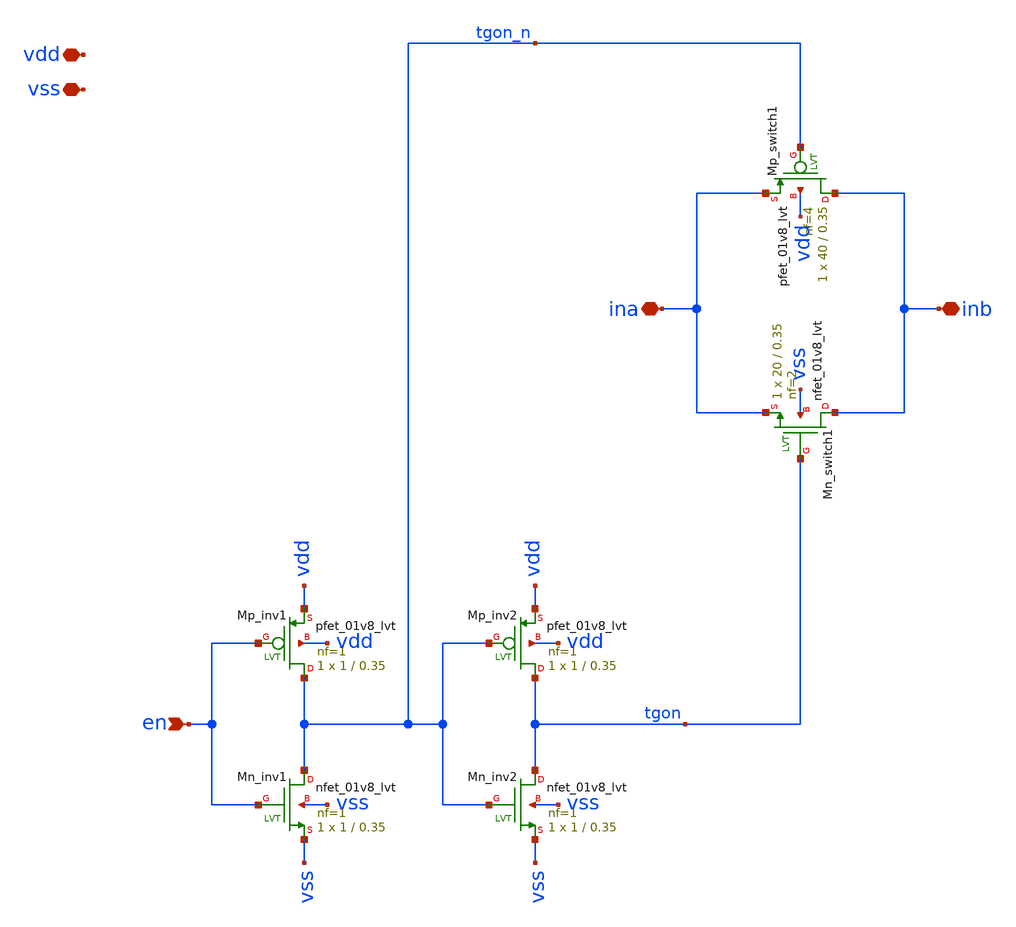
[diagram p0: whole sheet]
** sch_path: xsch/ip/tgates/tgate_1/tgate_1.sch
**.subckt tgate_1 vdd vss en inb ina
*.iopin vdd
*.iopin vss
*.ipin en
*.iopin inb
*.iopin ina
XMp_inv1 tgon_n en vdd vdd sky130_fd_pr__pfet_01v8_lvt L=0.35 W=1 nf=1 ad='int((nf+1)/2) * W/nf * 0.29'
+ as='int((nf+2)/2) * W/nf * 0.29' pd='2*int((nf+1)/2) * (W/nf + 0.29)' ps='2*int((nf+2)/2) * (W/nf + 0.29)'
+ nrd='0.29 / W' nrs='0.29 / W' sa=0 sb=0 sd=0 mult=1 m=1
XMn_inv1 tgon_n en vss vss sky130_fd_pr__nfet_01v8_lvt L=0.35 W=1 nf=1 ad='int((nf+1)/2) * W/nf * 0.29'
+ as='int((nf+2)/2) * W/nf * 0.29' pd='2*int((nf+1)/2) * (W/nf + 0.29)' ps='2*int((nf+2)/2) * (W/nf + 0.29)'
+ nrd='0.29 / W' nrs='0.29 / W' sa=0 sb=0 sd=0 mult=1 m=1
XMp_inv2 tgon tgon_n vdd vdd sky130_fd_pr__pfet_01v8_lvt L=0.35 W=1 nf=1 ad='int((nf+1)/2) * W/nf * 0.29'
+ as='int((nf+2)/2) * W/nf * 0.29' pd='2*int((nf+1)/2) * (W/nf + 0.29)' ps='2*int((nf+2)/2) * (W/nf + 0.29)'
+ nrd='0.29 / W' nrs='0.29 / W' sa=0 sb=0 sd=0 mult=1 m=1
XMn_inv2 tgon tgon_n vss vss sky130_fd_pr__nfet_01v8_lvt L=0.35 W=1 nf=1 ad='int((nf+1)/2) * W/nf * 0.29'
+ as='int((nf+2)/2) * W/nf * 0.29' pd='2*int((nf+1)/2) * (W/nf + 0.29)' ps='2*int((nf+2)/2) * (W/nf + 0.29)'
+ nrd='0.29 / W' nrs='0.29 / W' sa=0 sb=0 sd=0 mult=1 m=1
XMn_switch1 inb tgon ina vss sky130_fd_pr__nfet_01v8_lvt L=0.35 W=20 nf=2 ad='int((nf+1)/2) * W/nf * 0.29'
+ as='int((nf+2)/2) * W/nf * 0.29' pd='2*int((nf+1)/2) * (W/nf + 0.29)' ps='2*int((nf+2)/2) * (W/nf + 0.29)'
+ nrd='0.29 / W' nrs='0.29 / W' sa=0 sb=0 sd=0 mult=1 m=1
XMp_switch1 inb tgon_n ina vdd sky130_fd_pr__pfet_01v8_lvt L=0.35 W=40 nf=4 ad='int((nf+1)/2) * W/nf * 0.29'
+ as='int((nf+2)/2) * W/nf * 0.29' pd='2*int((nf+1)/2) * (W/nf + 0.29)' ps='2*int((nf+2)/2) * (W/nf + 0.29)'
+ nrd='0.29 / W' nrs='0.29 / W' sa=0 sb=0 sd=0 mult=1 m=1
**.ends
.end
